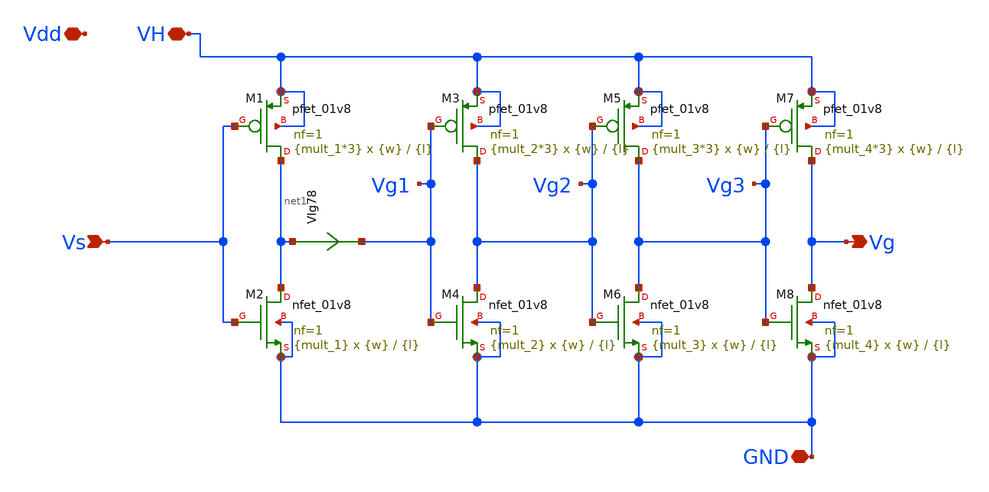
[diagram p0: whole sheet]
** sch_path: xschem/GD/GateDriver_woLS.sch
**.subckt GateDriver_woLS VH Vs Vg GND Vdd
*.iopin VH
*.ipin Vs
*.opin Vg
*.iopin GND
*.iopin Vdd
VIg78 net1 Vg1 0
.save i(vig78)
XM2 net1 Vs GND GND sky130_fd_pr__nfet_01v8 L={l} W={w} nf=1 ad='int((nf+1)/2) * W/nf * 0.29' as='int((nf+2)/2) * W/nf * 0.29'
+ pd='2*int((nf+1)/2) * (W/nf + 0.29)' ps='2*int((nf+2)/2) * (W/nf + 0.29)' nrd='0.29 / W' nrs='0.29 / W'
+ sa=0 sb=0 sd=0 mult={mult_1} m={mult_1}
XM1 net1 Vs VH VH sky130_fd_pr__pfet_01v8 L={l} W={w} nf=1 ad='int((nf+1)/2) * W/nf * 0.29' as='int((nf+2)/2) * W/nf * 0.29'
+ pd='2*int((nf+1)/2) * (W/nf + 0.29)' ps='2*int((nf+2)/2) * (W/nf + 0.29)' nrd='0.29 / W' nrs='0.29 / W'
+ sa=0 sb=0 sd=0 mult={mult_1*3} m={mult_1*3}
XM3 Vg2 Vg1 VH VH sky130_fd_pr__pfet_01v8 L={l} W={w} nf=1 ad='int((nf+1)/2) * W/nf * 0.29' as='int((nf+2)/2) * W/nf * 0.29'
+ pd='2*int((nf+1)/2) * (W/nf + 0.29)' ps='2*int((nf+2)/2) * (W/nf + 0.29)' nrd='0.29 / W' nrs='0.29 / W'
+ sa=0 sb=0 sd=0 mult={mult_2*3} m={mult_2*3}
XM4 Vg2 Vg1 GND GND sky130_fd_pr__nfet_01v8 L={l} W={w} nf=1 ad='int((nf+1)/2) * W/nf * 0.29' as='int((nf+2)/2) * W/nf * 0.29'
+ pd='2*int((nf+1)/2) * (W/nf + 0.29)' ps='2*int((nf+2)/2) * (W/nf + 0.29)' nrd='0.29 / W' nrs='0.29 / W'
+ sa=0 sb=0 sd=0 mult={mult_2} m={mult_2}
XM5 Vg3 Vg2 VH VH sky130_fd_pr__pfet_01v8 L={l} W={w} nf=1 ad='int((nf+1)/2) * W/nf * 0.29' as='int((nf+2)/2) * W/nf * 0.29'
+ pd='2*int((nf+1)/2) * (W/nf + 0.29)' ps='2*int((nf+2)/2) * (W/nf + 0.29)' nrd='0.29 / W' nrs='0.29 / W'
+ sa=0 sb=0 sd=0 mult={mult_3*3} m={mult_3*3}
XM6 Vg3 Vg2 GND GND sky130_fd_pr__nfet_01v8 L={l} W={w} nf=1 ad='int((nf+1)/2) * W/nf * 0.29' as='int((nf+2)/2) * W/nf * 0.29'
+ pd='2*int((nf+1)/2) * (W/nf + 0.29)' ps='2*int((nf+2)/2) * (W/nf + 0.29)' nrd='0.29 / W' nrs='0.29 / W'
+ sa=0 sb=0 sd=0 mult={mult_3} m={mult_3}
XM7 Vg Vg3 VH VH sky130_fd_pr__pfet_01v8 L={l} W={w} nf=1 ad='int((nf+1)/2) * W/nf * 0.29' as='int((nf+2)/2) * W/nf * 0.29'
+ pd='2*int((nf+1)/2) * (W/nf + 0.29)' ps='2*int((nf+2)/2) * (W/nf + 0.29)' nrd='0.29 / W' nrs='0.29 / W'
+ sa=0 sb=0 sd=0 mult={mult_4*3} m={mult_4*3}
XM8 Vg Vg3 GND GND sky130_fd_pr__nfet_01v8 L={l} W={w} nf=1 ad='int((nf+1)/2) * W/nf * 0.29' as='int((nf+2)/2) * W/nf * 0.29'
+ pd='2*int((nf+1)/2) * (W/nf + 0.29)' ps='2*int((nf+2)/2) * (W/nf + 0.29)' nrd='0.29 / W' nrs='0.29 / W'
+ sa=0 sb=0 sd=0 mult={mult_4} m={mult_4}
**.ends
.end
